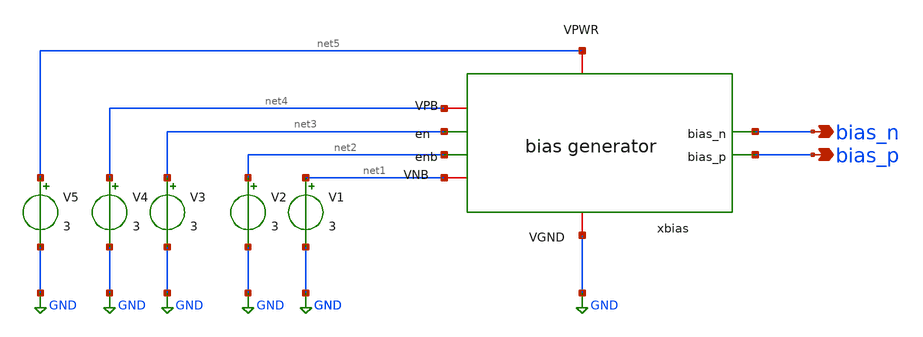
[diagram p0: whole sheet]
** sch_path: Team 2 Design/design_data/xschem/t2_bias_tb.sch
**.subckt t2_bias_tb bias_n bias_p
*.opin bias_n
*.opin bias_p
x1 net5 net4 GND net1 net3 bias_n bias_p net2 t2_bias
V1 net1 GND 3
V2 net2 GND 3
V3 net3 GND 3
V4 net4 GND 3
V5 net5 GND 3
**.ends

* expanding   symbol:  /foss/designs/cmos-pll-ihp-sg13g2/Team 2
*+ Design/design_data/xschem/t2_bias.sym # of pins=8
** sym_path: Team 2 Design/design_data/xschem/t2_bias.sym
** sch_path: Team 2 Design/design_data/xschem/t2_bias.sch
.subckt t2_bias VPWR VPB VGND VNB en bias_n bias_p enb
*.iopin VPWR
*.iopin VPB
*.iopin VGND
*.iopin VNB
*.ipin en
*.ipin enb
*.opin bias_n
*.opin bias_p
XM9 net1 en VPWR VPB sg13_lv_pmos w=0.5u l=0.15u ng=1 m=1 mm_ok=1
XM10 bias_p bias_p VPWR VPB sg13_lv_pmos w=2.0u l=1.0u ng=1 m=1 mm_ok=1
XM1 dio_mid dio_mid VPWR VPB sg13_lv_pmos w=0.5u l=0.15u ng=1 m=1 mm_ok=1
XM2 net1 net1 dio_mid VPB sg13_lv_pmos w=0.5u l=0.15u ng=1 m=1 mm_ok=1
XM3 bias_p en VPWR VPB sg13_lv_pmos w=0.5u l=0.15u ng=1 m=1 mm_ok=1
XM4 bias_n bias_p res_bot VPB sg13_lv_pmos w=2.0u l=1.0u ng=1 m=2 mm_ok=1
XM11 kick_sw en VGND VNB sg13_lv_nmos w=0.5u l=0.15u ng=1 m=1 mm_ok=1
XM12 bias_p net1 kick_sw VNB sg13_lv_nmos w=0.5u l=0.15u ng=1 m=1 mm_ok=1
XM5 net1 bias_n VGND VNB sg13_lv_nmos w=1.0u l=1.0u ng=1 m=1 mm_ok=1
XM6 bias_p bias_n VGND VNB sg13_lv_nmos w=1.0u l=1.0u ng=1 m=1 mm_ok=1
XM7 bias_n enb VGND VNB sg13_lv_nmos w=0.5u l=0.15u ng=1 m=1 mm_ok=1
XM8 bias_n bias_n VGND VNB sg13_lv_nmos w=1.0u l=1.0u ng=1 m=1 mm_ok=1
XR1 VPWR res_bot sub! rhigh w=0.5e-6 l=0.5e-6 m=1 b=0 mm_ok=1
.ends

.GLOBAL GND
.end
